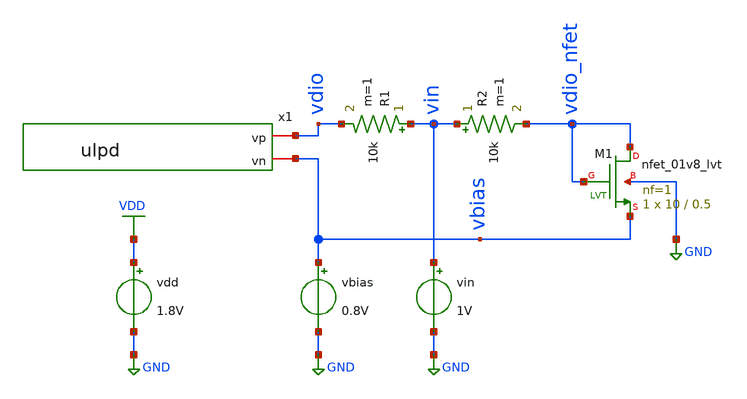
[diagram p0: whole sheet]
** sch_path: sample/ulpd/dc_sweep.sch
**.subckt dc_sweep
x1 vdio vbias ulpd
vin vin GND 1V
R1 vin vdio 10k m=1
vbias vbias GND 0.8V
R2 vin vdio_nfet 10k m=1
XM1 vdio_nfet vdio_nfet vbias GND sky130_fd_pr__nfet_01v8_lvt L=0.5 W=10 nf=1 ad='int((nf+1)/2) * W/nf * 0.29'
+ as='int((nf+2)/2) * W/nf * 0.29' pd='2*int((nf+1)/2) * (W/nf + 0.29)' ps='2*int((nf+2)/2) * (W/nf + 0.29)'
+ nrd='0.29 / W' nrs='0.29 / W' sa=0 sb=0 sd=0 mult=1 m=1
vdd VDD GND 1.8V
**** begin user architecture code


.param mc_mm_switch=0
.lib /home/matthias/pdk/sky130A/libs.tech/ngspice/sky130.lib.spice tt
.temp 100

.control
dc vin 0.01 2.0 0.01
plot   abs(v(vin)-v(vdio))/1e4+1e-15 vs v(vdio)-v(vbias)  abs(v(vin)-v(vdio_nfet))/1e4+1e-15 vs
+ v(vdio_nfet)-(vbias) ylog
.endc


**** end user architecture code
**.ends

* expanding   symbol:  /home/matthias/versuche/ulpd/ulpd.sym # of pins=2
** sym_path: sample/ulpd/ulpd.sym
** sch_path: sample/ulpd/ulpd.sch
.subckt ulpd vp vn
*.iopin vn
*.iopin vp
XM2 net1 vp vn GND sky130_fd_pr__nfet_01v8_lvt L=0.5 W=15 nf=10 ad='int((nf+1)/2) * W/nf * 0.29' as='int((nf+2)/2) * W/nf * 0.29'
+ pd='2*int((nf+1)/2) * (W/nf + 0.29)' ps='2*int((nf+2)/2) * (W/nf + 0.29)' nrd='0.29 / W' nrs='0.29 / W'
+ sa=0 sb=0 sd=0 mult=1 m=1
XM1 net1 vn vp VDD sky130_fd_pr__pfet_01v8_lvt L=0.5 W=20 nf=10 ad='int((nf+1)/2) * W/nf * 0.29' as='int((nf+2)/2) * W/nf * 0.29'
+ pd='2*int((nf+1)/2) * (W/nf + 0.29)' ps='2*int((nf+2)/2) * (W/nf + 0.29)' nrd='0.29 / W' nrs='0.29 / W'
+ sa=0 sb=0 sd=0 mult=1 m=1
.ends

.GLOBAL GND
.GLOBAL VDD
.end
